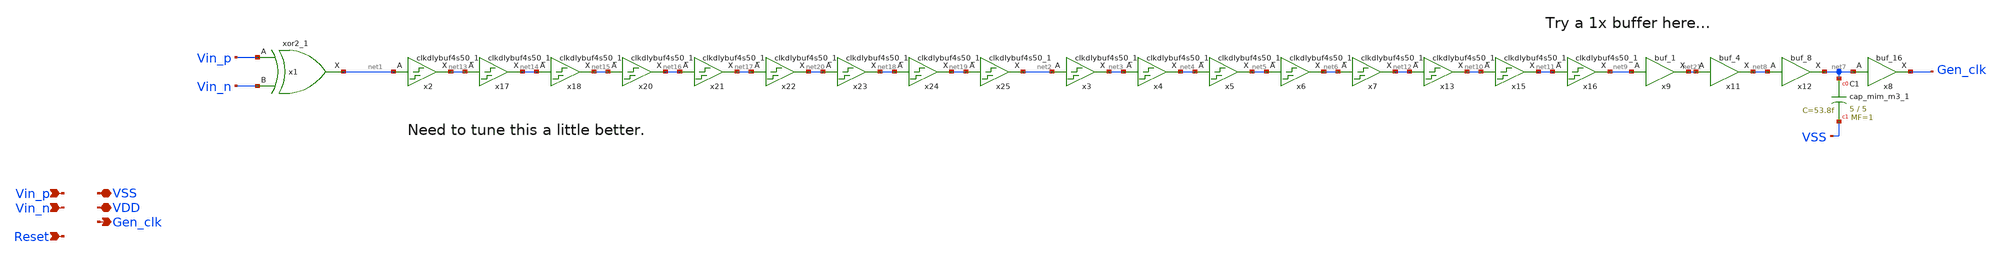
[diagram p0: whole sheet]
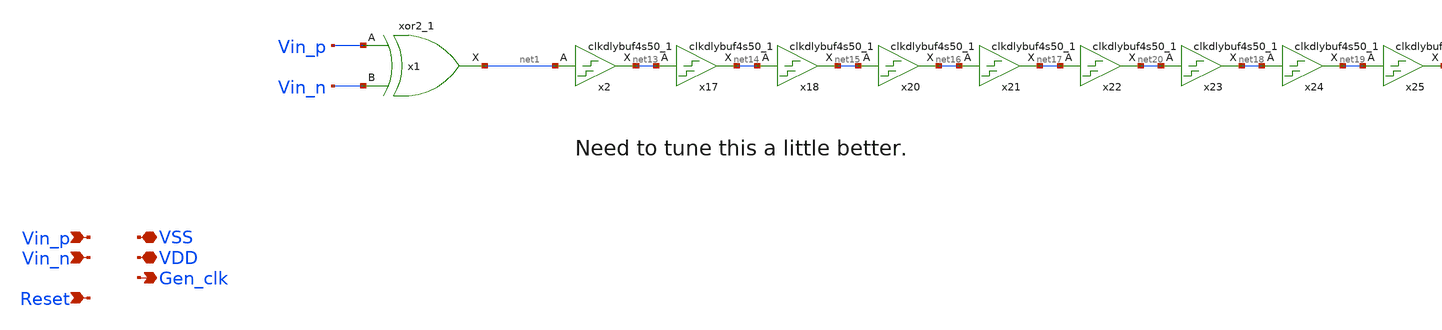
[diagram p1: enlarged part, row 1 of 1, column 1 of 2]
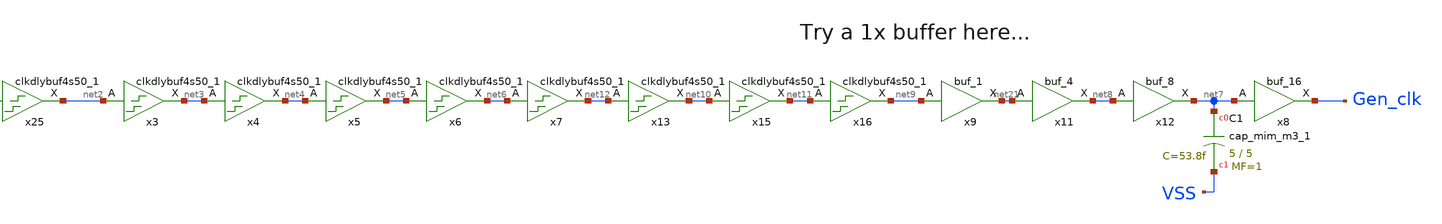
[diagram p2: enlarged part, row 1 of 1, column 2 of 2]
** sch_path: xschem/src/xor_clock_gen/xor_clock_gen_normal_buf.sch
**.subckt xor_clock_gen_normal_buf Vin_p VSS Gen_clk VDD Vin_n Reset
*.ipin Vin_p
*.iopin VSS
*.opin Gen_clk
*.iopin VDD
*.ipin Vin_n
*.ipin Reset
x1 Vin_p Vin_n VSS VSS VDD VDD net1 sky130_fd_sc_hd__xor2_1
x2 net1 VSS VSS VDD VDD net13 sky130_fd_sc_hd__clkdlybuf4s50_1
x3 net2 VSS VSS VDD VDD net3 sky130_fd_sc_hd__clkdlybuf4s50_1
x4 net3 VSS VSS VDD VDD net4 sky130_fd_sc_hd__clkdlybuf4s50_1
x5 net4 VSS VSS VDD VDD net5 sky130_fd_sc_hd__clkdlybuf4s50_1
x6 net5 VSS VSS VDD VDD net6 sky130_fd_sc_hd__clkdlybuf4s50_1
x7 net6 VSS VSS VDD VDD net12 sky130_fd_sc_hd__clkdlybuf4s50_1
x8 net7 VSS VSS VDD VDD Gen_clk sky130_fd_sc_hd__buf_16
x11 net21 VSS VSS VDD VDD net8 sky130_fd_sc_hd__buf_4
x12 net8 VSS VSS VDD VDD net7 sky130_fd_sc_hd__buf_8
x13 net12 VSS VSS VDD VDD net10 sky130_fd_sc_hd__clkdlybuf4s50_1
x15 net10 VSS VSS VDD VDD net11 sky130_fd_sc_hd__clkdlybuf4s50_1
x16 net11 VSS VSS VDD VDD net9 sky130_fd_sc_hd__clkdlybuf4s50_1
x17 net13 VSS VSS VDD VDD net14 sky130_fd_sc_hd__clkdlybuf4s50_1
x18 net14 VSS VSS VDD VDD net15 sky130_fd_sc_hd__clkdlybuf4s50_1
x20 net15 VSS VSS VDD VDD net16 sky130_fd_sc_hd__clkdlybuf4s50_1
x21 net16 VSS VSS VDD VDD net17 sky130_fd_sc_hd__clkdlybuf4s50_1
x22 net17 VSS VSS VDD VDD net20 sky130_fd_sc_hd__clkdlybuf4s50_1
x23 net20 VSS VSS VDD VDD net18 sky130_fd_sc_hd__clkdlybuf4s50_1
x24 net18 VSS VSS VDD VDD net19 sky130_fd_sc_hd__clkdlybuf4s50_1
x25 net19 VSS VSS VDD VDD net2 sky130_fd_sc_hd__clkdlybuf4s50_1
x9 net9 VSS VSS VDD VDD net21 sky130_fd_sc_hd__buf_1
XC1 net7 VSS sky130_fd_pr__cap_mim_m3_1 W=5 L=5 MF=1 m=1
**.ends
.end
